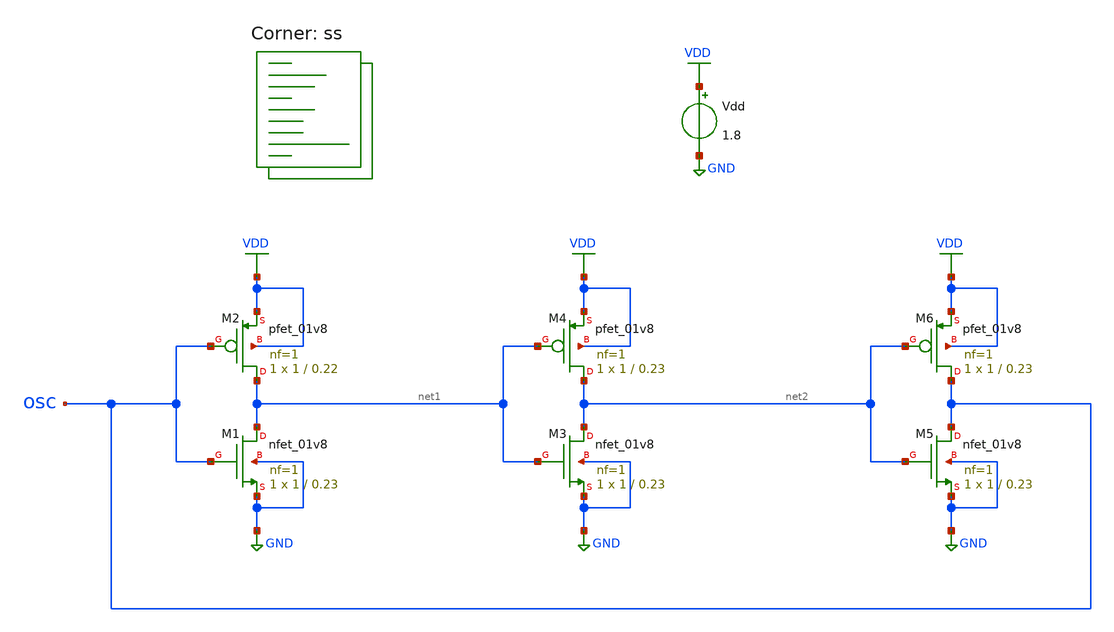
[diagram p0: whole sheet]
** sch_path: projects/pll/bandgapref/xschem_ngspice/test_inverter_speed.sch
**.subckt test_inverter_speed
Vdd VDD GND 1.8
XM1 net1 osc GND GND sky130_fd_pr__nfet_01v8 L=0.23 W=1 nf=1 ad='int((nf+1)/2) * W/nf * 0.29' as='int((nf+2)/2) * W/nf * 0.29'
+ pd='2*int((nf+1)/2) * (W/nf + 0.29)' ps='2*int((nf+2)/2) * (W/nf + 0.29)' nrd='0.29 / W' nrs='0.29 / W'
+ sa=0 sb=0 sd=0 mult=1 m=1
XM2 net1 osc VDD VDD sky130_fd_pr__pfet_01v8 L=0.22 W=1 nf=1 ad='int((nf+1)/2) * W/nf * 0.29' as='int((nf+2)/2) * W/nf * 0.29'
+ pd='2*int((nf+1)/2) * (W/nf + 0.29)' ps='2*int((nf+2)/2) * (W/nf + 0.29)' nrd='0.29 / W' nrs='0.29 / W'
+ sa=0 sb=0 sd=0 mult=1 m=1
XM3 net2 net1 GND GND sky130_fd_pr__nfet_01v8 L=0.23 W=1 nf=1 ad='int((nf+1)/2) * W/nf * 0.29' as='int((nf+2)/2) * W/nf * 0.29'
+ pd='2*int((nf+1)/2) * (W/nf + 0.29)' ps='2*int((nf+2)/2) * (W/nf + 0.29)' nrd='0.29 / W' nrs='0.29 / W'
+ sa=0 sb=0 sd=0 mult=1 m=1
XM4 net2 net1 VDD VDD sky130_fd_pr__pfet_01v8 L=0.23 W=1 nf=1 ad='int((nf+1)/2) * W/nf * 0.29' as='int((nf+2)/2) * W/nf * 0.29'
+ pd='2*int((nf+1)/2) * (W/nf + 0.29)' ps='2*int((nf+2)/2) * (W/nf + 0.29)' nrd='0.29 / W' nrs='0.29 / W'
+ sa=0 sb=0 sd=0 mult=1 m=1
XM5 osc net2 GND GND sky130_fd_pr__nfet_01v8 L=0.23 W=1 nf=1 ad='int((nf+1)/2) * W/nf * 0.29' as='int((nf+2)/2) * W/nf * 0.29'
+ pd='2*int((nf+1)/2) * (W/nf + 0.29)' ps='2*int((nf+2)/2) * (W/nf + 0.29)' nrd='0.29 / W' nrs='0.29 / W'
+ sa=0 sb=0 sd=0 mult=1 m=1
XM6 osc net2 VDD VDD sky130_fd_pr__pfet_01v8 L=0.23 W=1 nf=1 ad='int((nf+1)/2) * W/nf * 0.29' as='int((nf+2)/2) * W/nf * 0.29'
+ pd='2*int((nf+1)/2) * (W/nf + 0.29)' ps='2*int((nf+2)/2) * (W/nf + 0.29)' nrd='0.29 / W' nrs='0.29 / W'
+ sa=0 sb=0 sd=0 mult=1 m=1
**** begin user architecture code
.lib $::SKYWATER_MODELS/sky130.lib.spice ss



.option method=gear
.option wnflag=1
.option savecurrents

.save @m.xm1.msky130_fd_pr__nfet_01v8[gm] @m.xm2.msky130_fd_pr__pfet_01v8[gm] @m.xm3.msky130_fd_pr__nfet_01v8[gm] @m.xm4.msky130_fd_pr__pfet_01v8[gm] @m.xm5.msky130_fd_pr__nfet_01v8[gm] @m.xm6.msky130_fd_pr__pfet_01v8[gm]

.temp 75
.ic v(osc)=0
.option INTERP

.control
  save all
  tran 0.01ps 3ns
  remzerovec
  linearize v(osc)
  set specwindow=blackman
  fft v(osc)
  print vdb(osc)

  write test_inverter_speed.raw
  set appendwrite
.endc




**** end user architecture code
**.ends
.GLOBAL VDD
.GLOBAL GND
.end
